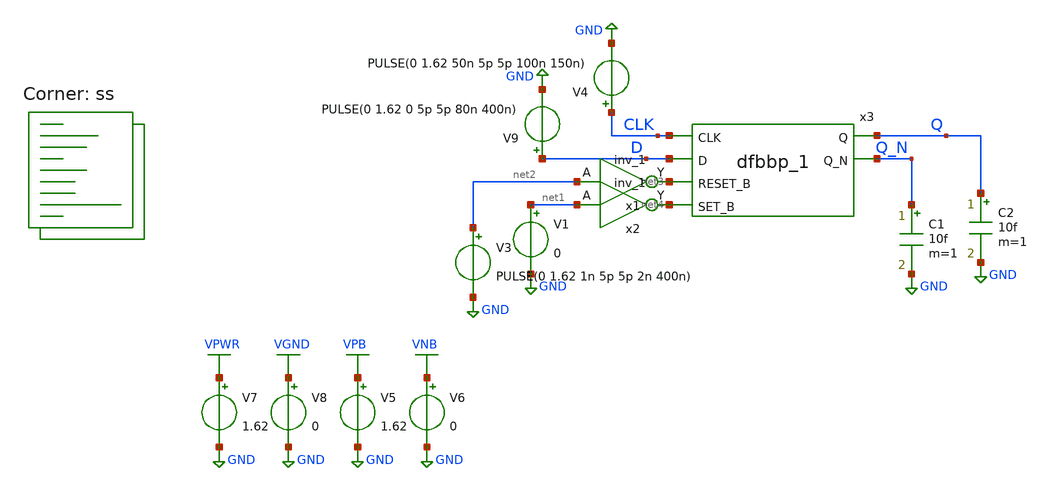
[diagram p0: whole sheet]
** sch_path: hgu/tb/tb_hgu_dfbbp_1.sch
**.subckt tb_hgu_dfbbp_1
x1 net2 VGND VNB VPB VPWR net3 sky130_fd_sc_hd__inv_1
x2 net1 VGND VNB VPB VPWR net4 sky130_fd_sc_hd__inv_1
V1 net1 GND 0
V3 net2 GND PULSE(0 1.62 1n 5p 5p 2n 400n)
V4 CLK GND PULSE(0 1.62 50n 5p 5p 100n 150n)
C1 Q_N GND 10f m=1
C2 Q GND 10f m=1
x3 CLK D net3 net4 VGND VNB VPB VPWR Q Q_N sky130_fd_sc_hd__dfbbp_1
V5 VPB GND 1.62
V6 VNB GND 0
V7 VPWR GND 1.62
V8 VGND GND 0
V9 D GND PULSE(0 1.62 0 5p 5p 80n 400n)
**** begin user architecture code


.save all
.temp = 100
.tran 100p 400n
.OPTIONS savecurrent
.include /foss/pdks/sky130A/libs.ref/sky130_fd_sc_hd/spice/sky130_fd_sc_hd.spice
.control
	run
	let svdd = 1.62
	let max = svdd*0.8
	let min = svdd*0.2
	let mid = svdd*0.5
	meas tran rising_s find time when V(q)=min RISE=1 TD=1000p
        meas tran rising_e find time when V(q)=max RISE=1 TD=1000p
        let rising_time = rising_e-rising_s
        meas tran falling_s find time when V(q)=max FALL=1 TD=1000p
        meas tran falling_e find time when V(q)=min FALL=1 TD=1000p
        let falling_time = falling_e-falling_s
        meas tran IN find time when V(clk)=mid RISE=1 TD=1000p
        meas tran OUT find time when V(q)=mid RISE=1 TD=1000p
        let rising_delay = OUT-IN
	meas tran fIN find time when V(clk)=mid RISE=1 TD=100n
        meas tran fOUT find time when V(q)=mid FALL=1 TD=100n
        let falling_delay = fOUT-fIN

        print rising_time falling_time rising_delay falling_delay

	plot v(CLK)+4 V(D)+2 V(Q)
.endc


.lib $::SKYWATER_MODELS/sky130.lib.spice ss
**** end user architecture code
**.ends
.GLOBAL GND
.GLOBAL VPB
.GLOBAL VNB
.GLOBAL VPWR
.GLOBAL VGND
.end
